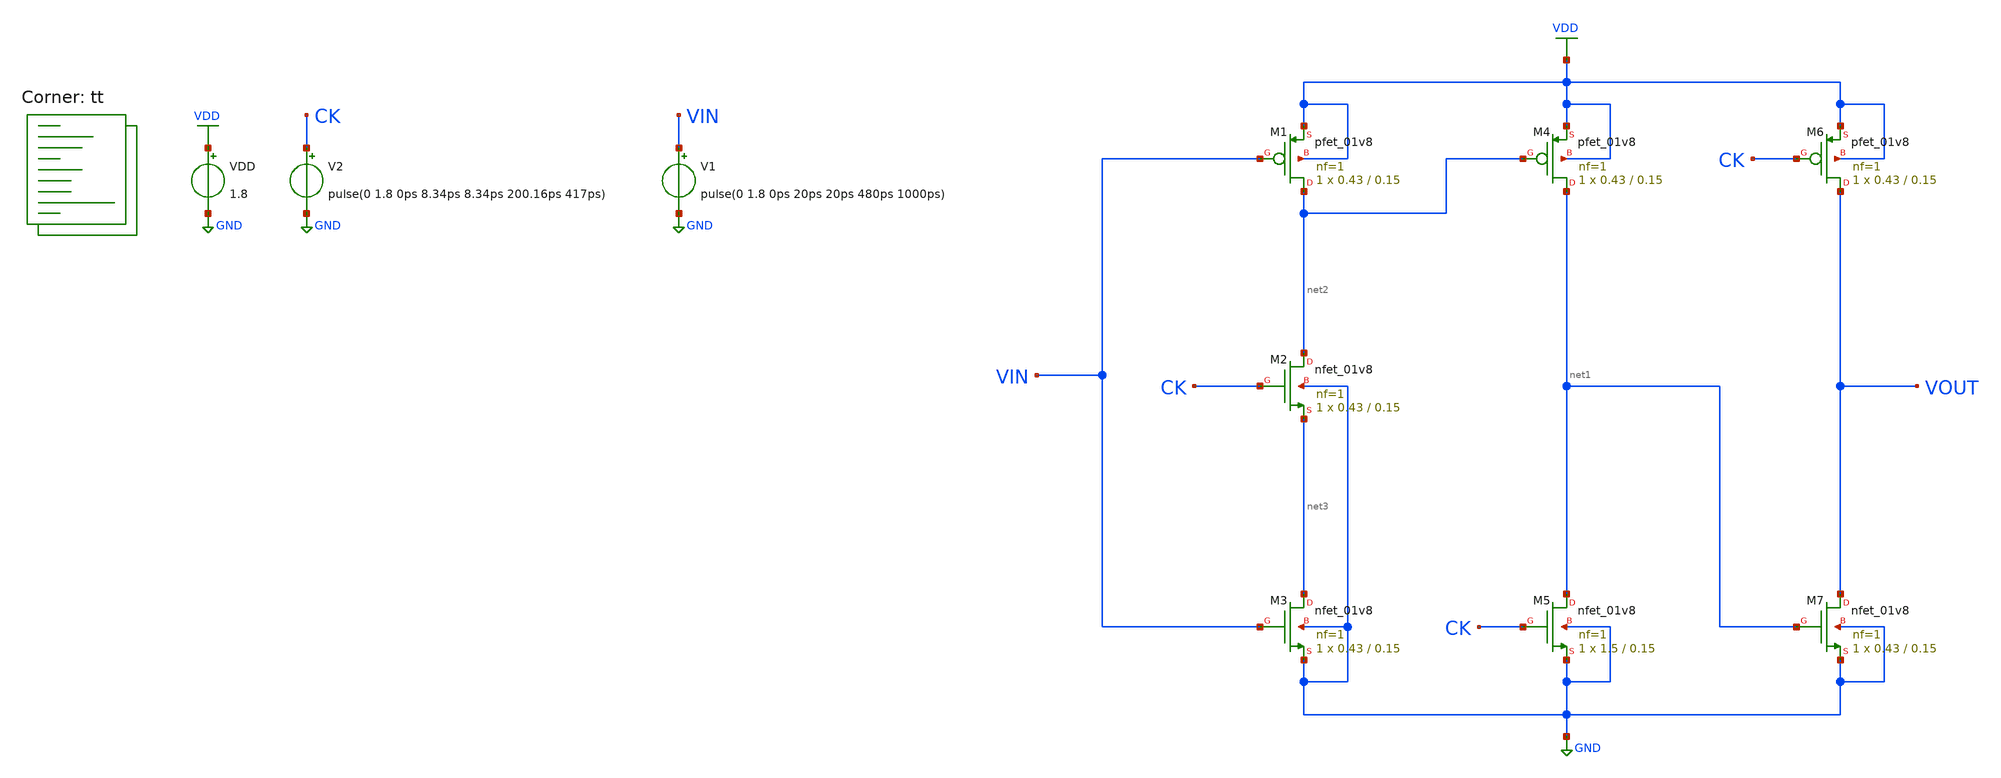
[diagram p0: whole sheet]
** sch_path: projects/pll/divider/xschem_ngspice/tb_TSPC_FF_ratioed.sch
**.subckt tb_TSPC_FF_ratioed
VDD VDD GND 1.8
XM6 VOUT CK VDD VDD sky130_fd_pr__pfet_01v8 L=0.15 W=0.43 nf=1 ad='int((nf+1)/2) * W/nf * 0.29' as='int((nf+2)/2) * W/nf * 0.29'
+ pd='2*int((nf+1)/2) * (W/nf + 0.29)' ps='2*int((nf+2)/2) * (W/nf + 0.29)' nrd='0.29 / W' nrs='0.29 / W'
+ sa=0 sb=0 sd=0 mult=1 m=1
XM7 VOUT net1 GND GND sky130_fd_pr__nfet_01v8 L=0.15 W=0.43 nf=1 ad='int((nf+1)/2) * W/nf * 0.29' as='int((nf+2)/2) * W/nf * 0.29'
+ pd='2*int((nf+1)/2) * (W/nf + 0.29)' ps='2*int((nf+2)/2) * (W/nf + 0.29)' nrd='0.29 / W' nrs='0.29 / W'
+ sa=0 sb=0 sd=0 mult=1 m=1
XM4 net1 net2 VDD VDD sky130_fd_pr__pfet_01v8 L=0.15 W=0.43 nf=1 ad='int((nf+1)/2) * W/nf * 0.29' as='int((nf+2)/2) * W/nf * 0.29'
+ pd='2*int((nf+1)/2) * (W/nf + 0.29)' ps='2*int((nf+2)/2) * (W/nf + 0.29)' nrd='0.29 / W' nrs='0.29 / W'
+ sa=0 sb=0 sd=0 mult=1 m=1
XM5 net1 CK GND GND sky130_fd_pr__nfet_01v8 L=0.15 W=1.5 nf=1 ad='int((nf+1)/2) * W/nf * 0.29' as='int((nf+2)/2) * W/nf * 0.29'
+ pd='2*int((nf+1)/2) * (W/nf + 0.29)' ps='2*int((nf+2)/2) * (W/nf + 0.29)' nrd='0.29 / W' nrs='0.29 / W'
+ sa=0 sb=0 sd=0 mult=1 m=1
XM1 net2 VIN VDD VDD sky130_fd_pr__pfet_01v8 L=0.15 W=0.43 nf=1 ad='int((nf+1)/2) * W/nf * 0.29' as='int((nf+2)/2) * W/nf * 0.29'
+ pd='2*int((nf+1)/2) * (W/nf + 0.29)' ps='2*int((nf+2)/2) * (W/nf + 0.29)' nrd='0.29 / W' nrs='0.29 / W'
+ sa=0 sb=0 sd=0 mult=1 m=1
XM3 net3 VIN GND GND sky130_fd_pr__nfet_01v8 L=0.15 W=0.43 nf=1 ad='int((nf+1)/2) * W/nf * 0.29' as='int((nf+2)/2) * W/nf * 0.29'
+ pd='2*int((nf+1)/2) * (W/nf + 0.29)' ps='2*int((nf+2)/2) * (W/nf + 0.29)' nrd='0.29 / W' nrs='0.29 / W'
+ sa=0 sb=0 sd=0 mult=1 m=1
XM2 net2 CK net3 GND sky130_fd_pr__nfet_01v8 L=0.15 W=0.43 nf=1 ad='int((nf+1)/2) * W/nf * 0.29' as='int((nf+2)/2) * W/nf * 0.29'
+ pd='2*int((nf+1)/2) * (W/nf + 0.29)' ps='2*int((nf+2)/2) * (W/nf + 0.29)' nrd='0.29 / W' nrs='0.29 / W'
+ sa=0 sb=0 sd=0 mult=1 m=1
V2 CK GND pulse(0 1.8 0ps 8.34ps 8.34ps 200.16ps 417ps)
V1 VIN GND pulse(0 1.8 0ps 20ps 20ps 480ps 1000ps)
**** begin user architecture code



.option method=gear
.option wnflag=1

.control

  save all
  tran 5p 20n
  remzerovec
  write tb_TSPC_FF_ratioed.raw
  set appendwrite

.endc



.lib $::SKYWATER_MODELS/sky130.lib.spice tt
**** end user architecture code
**.ends
.GLOBAL GND
.GLOBAL VDD
.end
